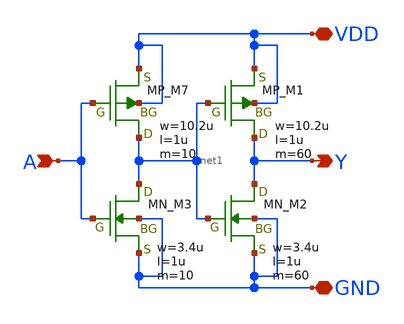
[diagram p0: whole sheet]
** sch_path: libs.tech/xschem/TR-1um_5_stdcell/CLKBUF_X12.sch
**.subckt CLKBUF_X12 A Y VDD GND
*.ipin A
*.opin Y
*.iopin VDD
*.iopin GND
XM7 net1 A VDD VDD PMOS w=10.2u l=1u nrd=0 nrs=0 m=10
XM1 Y net1 VDD VDD PMOS w=10.2u l=1u nrd=0 nrs=0 m=60
XM3 net1 A GND GND NMOS w=3.4u l=1u nrd=0 nrs=0 m=10
XM2 Y net1 GND GND NMOS w=3.4u l=1u nrd=0 nrs=0 m=60
**.ends
.end
